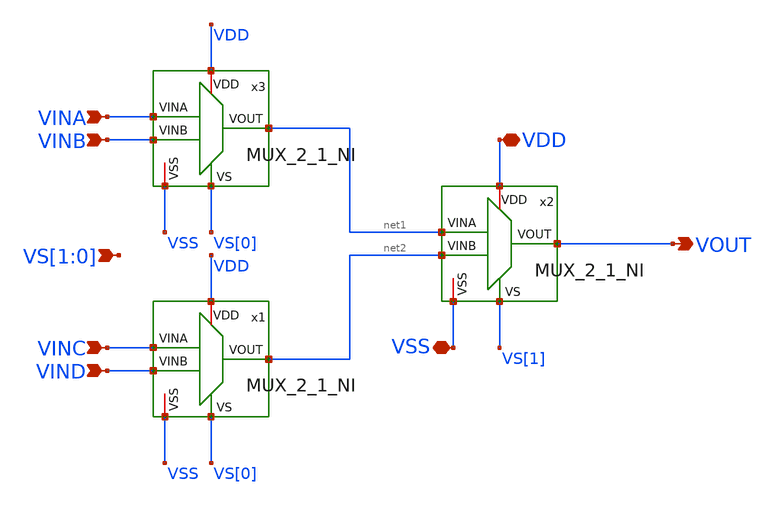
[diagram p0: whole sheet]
** sch_path: ADC8711-main/schematic/xschem/MUX_4_1_NI.sch
**.subckt MUX_4_1_NI VOUT VDD VSS VINA VINB VINC VIND VS[1],VS[0]
*.opin VOUT
*.iopin VDD
*.iopin VSS
*.ipin VINA
*.ipin VINB
*.ipin VINC
*.ipin VIND
*.ipin VS[1],VS[0]
x3 VDD VINA net1 VS[0] VINB VSS MUX_2_1_NI
x1 VDD VINC net2 VS[0] VIND VSS MUX_2_1_NI
x2 VDD net1 VOUT VS[1] net2 VSS MUX_2_1_NI
**.ends
.end
